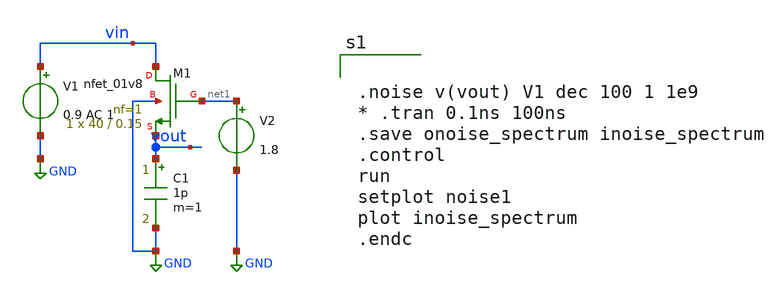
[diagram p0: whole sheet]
** sch_path: xschem/shn_test.sch
**.subckt shn_test
C1 vout GND 1p m=1
V1 vin GND 0.9 AC 1
XM1 vin net1 vout GND sky130_fd_pr__nfet_01v8 L=0.15 W=40 nf=1 ad='int((nf+1)/2) * W/nf * 0.29' as='int((nf+2)/2) * W/nf * 0.29'
+ pd='2*int((nf+1)/2) * (W/nf + 0.29)' ps='2*int((nf+2)/2) * (W/nf + 0.29)' nrd='0.29 / W' nrs='0.29 / W'
+ sa=0 sb=0 sd=0 mult=1 m=1
V2 net1 GND 1.8
**** begin user architecture code
.lib $::SKYWATER_MODELS/sky130.lib.spice tt
.include $::PDKPATH/libs.ref/sky130_fd_sc_hs/spice/sky130_fd_sc_hs.spice



.noise v(vout) V1 dec 100 1 1e9
* .tran 0.1ns 100ns
.save onoise_spectrum inoise_spectrum
.control
run
setplot noise1
plot inoise_spectrum
.endc


**** end user architecture code
**.ends
.GLOBAL GND
.end
